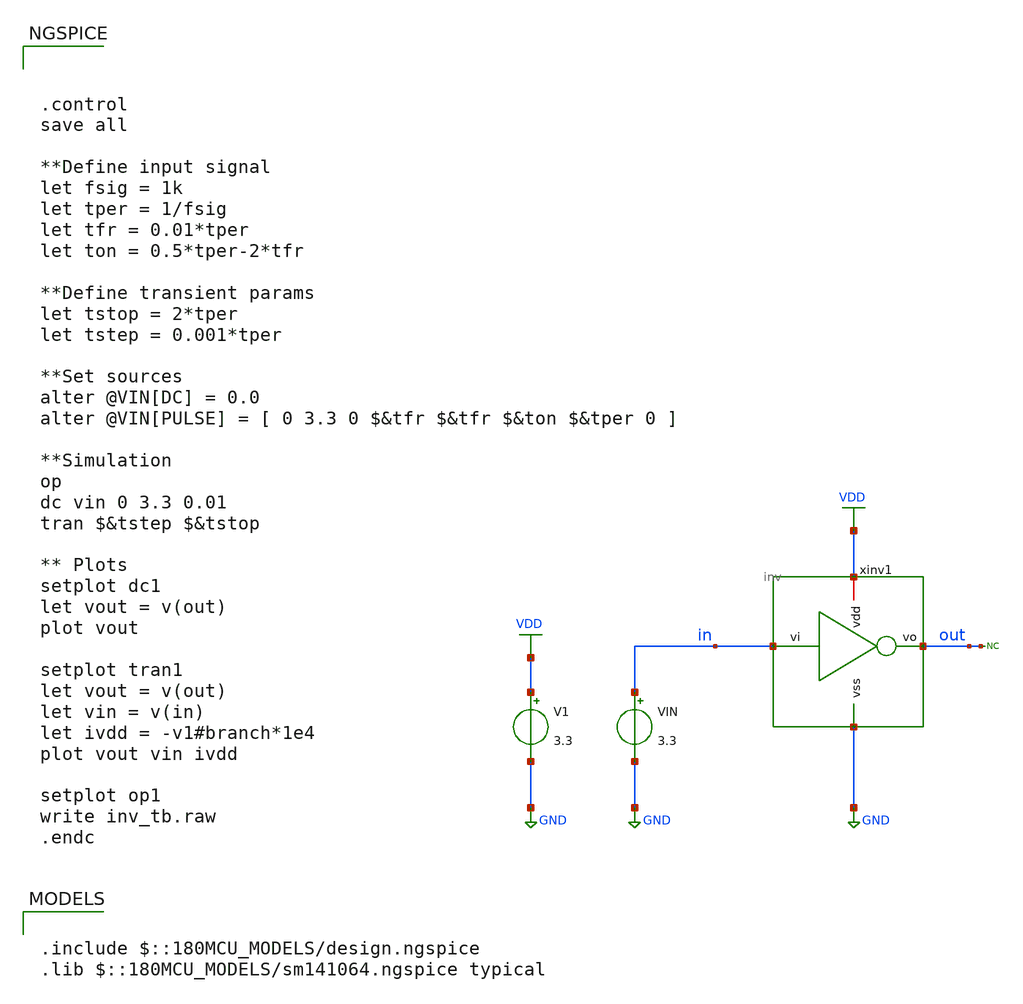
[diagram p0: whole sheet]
** sch_path: designs/inv_tb.sch
**.subckt inv_tb
xinv1 VDD in out GND inv
V1 VDD GND 3.3
VIN in GND 3.3
* noconn out
**** begin user architecture code



.control
save all

**Define input signal
let fsig = 1k
let tper = 1/fsig
let tfr = 0.01*tper
let ton = 0.5*tper-2*tfr

**Define transient params
let tstop = 2*tper
let tstep = 0.001*tper

**Set sources
alter @VIN[DC] = 0.0
alter @VIN[PULSE] = [ 0 3.3 0 $&tfr $&tfr $&ton $&tper 0 ]

**Simulation
op
dc vin 0 3.3 0.01
tran $&tstep $&tstop

** Plots
setplot dc1
let vout = v(out)
plot vout

setplot tran1
let vout = v(out)
let vin = v(in)
let ivdd = -v1#branch*1e4
plot vout vin ivdd

setplot op1
write inv_tb.raw
.endc



.include $::180MCU_MODELS/design.ngspice
.lib $::180MCU_MODELS/sm141064.ngspice typical

**** end user architecture code
**.ends

* expanding   symbol:  inv.sym # of pins=4
** sym_path: designs/inv.sym
** sch_path: designs/inv.sch
.subckt inv vdd vi vo vss
*.iopin vdd
*.ipin vss
*.ipin vi
*.opin vo
XM1 vo vi vss vss nfet_03v3 L=0.28u W=1u nf=1 ad='int((nf+1)/2) * W/nf * 0.18u' as='int((nf+2)/2) * W/nf * 0.18u'
+ pd='2*int((nf+1)/2) * (W/nf + 0.18u)' ps='2*int((nf+2)/2) * (W/nf + 0.18u)' nrd='0.18u / W' nrs='0.18u / W'
+ sa=0 sb=0 sd=0 m=1
XM2 vo vi vdd vdd pfet_03v3 L=0.28u W=2u nf=1 ad='int((nf+1)/2) * W/nf * 0.18u' as='int((nf+2)/2) * W/nf * 0.18u'
+ pd='2*int((nf+1)/2) * (W/nf + 0.18u)' ps='2*int((nf+2)/2) * (W/nf + 0.18u)' nrd='0.18u / W' nrs='0.18u / W'
+ sa=0 sb=0 sd=0 m=1
.ends

.GLOBAL VDD
.GLOBAL GND
.end
